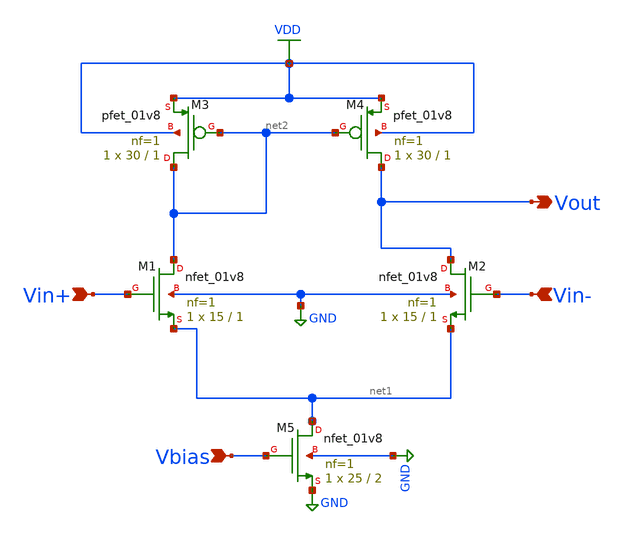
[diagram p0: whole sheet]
** sch_path: analog/schematics/bootcamp_opamp.sch
**.subckt bootcamp_opamp Vin+ Vbias Vin- Vout
*.ipin Vin+
*.ipin Vbias
*.ipin Vin-
*.opin Vout
XM1 net2 Vin+ net1 GND sky130_fd_pr__nfet_01v8 L=1 W=15 nf=1 ad='int((nf+1)/2) * W/nf * 0.29' as='int((nf+2)/2) * W/nf * 0.29'
+ pd='2*int((nf+1)/2) * (W/nf + 0.29)' ps='2*int((nf+2)/2) * (W/nf + 0.29)' nrd='0.29 / W' nrs='0.29 / W'
+ sa=0 sb=0 sd=0 mult=1 m=1
XM3 net2 net2 VDD VDD sky130_fd_pr__pfet_01v8 L=1 W=30 nf=1 ad='int((nf+1)/2) * W/nf * 0.29' as='int((nf+2)/2) * W/nf * 0.29'
+ pd='2*int((nf+1)/2) * (W/nf + 0.29)' ps='2*int((nf+2)/2) * (W/nf + 0.29)' nrd='0.29 / W' nrs='0.29 / W'
+ sa=0 sb=0 sd=0 mult=1 m=1
XM4 Vout net2 VDD VDD sky130_fd_pr__pfet_01v8 L=1 W=30 nf=1 ad='int((nf+1)/2) * W/nf * 0.29' as='int((nf+2)/2) * W/nf * 0.29'
+ pd='2*int((nf+1)/2) * (W/nf + 0.29)' ps='2*int((nf+2)/2) * (W/nf + 0.29)' nrd='0.29 / W' nrs='0.29 / W'
+ sa=0 sb=0 sd=0 mult=1 m=1
XM5 net1 Vbias GND GND sky130_fd_pr__nfet_01v8 L=2 W=25 nf=1 ad='int((nf+1)/2) * W/nf * 0.29' as='int((nf+2)/2) * W/nf * 0.29'
+ pd='2*int((nf+1)/2) * (W/nf + 0.29)' ps='2*int((nf+2)/2) * (W/nf + 0.29)' nrd='0.29 / W' nrs='0.29 / W'
+ sa=0 sb=0 sd=0 mult=1 m=1
XM2 Vout Vin- net1 GND sky130_fd_pr__nfet_01v8 L=1 W=15 nf=1 ad='int((nf+1)/2) * W/nf * 0.29' as='int((nf+2)/2) * W/nf * 0.29'
+ pd='2*int((nf+1)/2) * (W/nf + 0.29)' ps='2*int((nf+2)/2) * (W/nf + 0.29)' nrd='0.29 / W' nrs='0.29 / W'
+ sa=0 sb=0 sd=0 mult=1 m=1
**.ends
.GLOBAL GND
.GLOBAL VDD
.end
